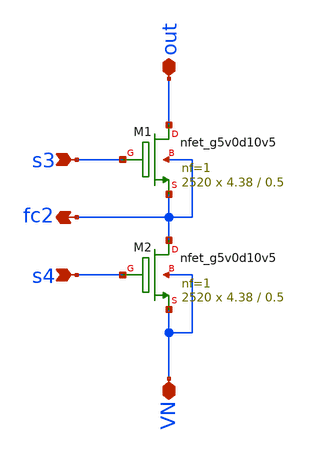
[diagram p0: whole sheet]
** sch_path: xschem/hierarchy_sch/transistor_group_two.sch
**.subckt transistor_group_two out s3 s4 fc2 VN
*.iopin out
*.ipin s3
*.ipin s4
*.opin fc2
*.iopin VN
XM1 out s3 fc2 fc2 sky130_fd_pr__nfet_g5v0d10v5 L=0.5 W=4.38 nf=1 ad='int((nf+1)/2) * W/nf * 0.29' as='int((nf+2)/2) * W/nf * 0.29'
+ pd='2*int((nf+1)/2) * (W/nf + 0.29)' ps='2*int((nf+2)/2) * (W/nf + 0.29)' nrd='0.29 / W' nrs='0.29 / W'
+ sa=0 sb=0 sd=0 mult=2520 m=2520
XM2 fc2 s4 VN VN sky130_fd_pr__nfet_g5v0d10v5 L=0.5 W=4.38 nf=1 ad='int((nf+1)/2) * W/nf * 0.29' as='int((nf+2)/2) * W/nf * 0.29'
+ pd='2*int((nf+1)/2) * (W/nf + 0.29)' ps='2*int((nf+2)/2) * (W/nf + 0.29)' nrd='0.29 / W' nrs='0.29 / W'
+ sa=0 sb=0 sd=0 mult=2520 m=2520
**.ends
.end
